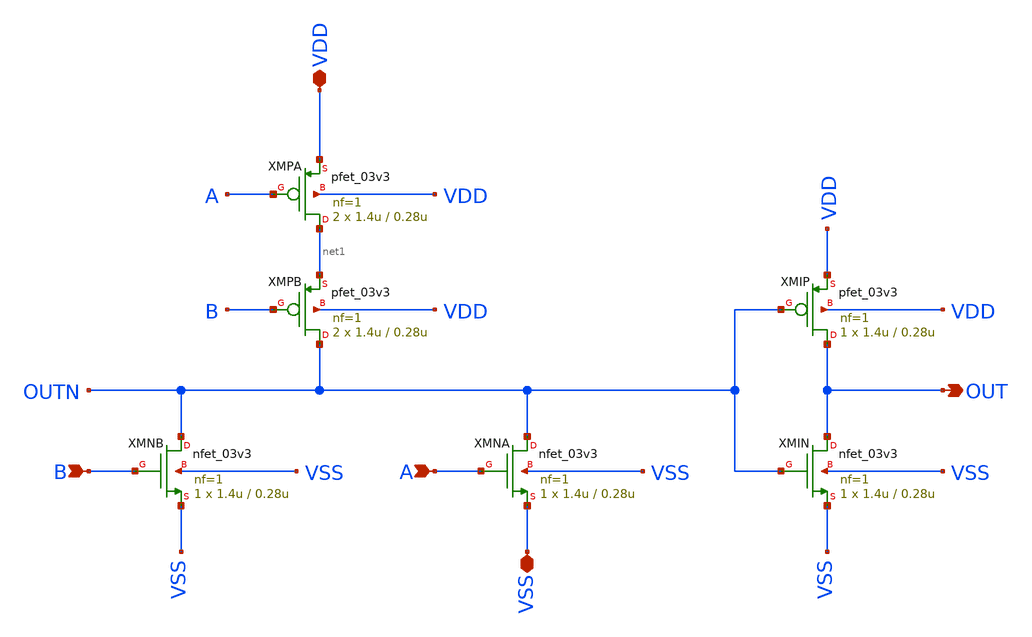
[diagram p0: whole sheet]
** sch_path: designs/gate_or/xschem/gate_or.sch
**.subckt gate_or OUT A VDD VSS B
*.opin OUT
*.ipin A
*.iopin VDD
*.iopin VSS
*.ipin B
XMNB OUTN B VSS VSS nfet_03v3 L=0.28u W=1.4u nf=1 ad='int((nf+1)/2) * W/nf * 0.18u' as='int((nf+2)/2) * W/nf * 0.18u'
+ pd='2*int((nf+1)/2) * (W/nf + 0.18u)' ps='2*int((nf+2)/2) * (W/nf + 0.18u)' nrd='0.18u / W' nrs='0.18u / W'
+ sa=0 sb=0 sd=0 m=1
XMPB OUTN B net1 VDD pfet_03v3 L=0.28u W=1.4u nf=1 ad='int((nf+1)/2) * W/nf * 0.18u' as='int((nf+2)/2) * W/nf * 0.18u'
+ pd='2*int((nf+1)/2) * (W/nf + 0.18u)' ps='2*int((nf+2)/2) * (W/nf + 0.18u)' nrd='0.18u / W' nrs='0.18u / W'
+ sa=0 sb=0 sd=0 m=2
XMNA OUTN A VSS VSS nfet_03v3 L=0.28u W=1.4u nf=1 ad='int((nf+1)/2) * W/nf * 0.18u' as='int((nf+2)/2) * W/nf * 0.18u'
+ pd='2*int((nf+1)/2) * (W/nf + 0.18u)' ps='2*int((nf+2)/2) * (W/nf + 0.18u)' nrd='0.18u / W' nrs='0.18u / W'
+ sa=0 sb=0 sd=0 m=1
XMPA net1 A VDD VDD pfet_03v3 L=0.28u W=1.4u nf=1 ad='int((nf+1)/2) * W/nf * 0.18u' as='int((nf+2)/2) * W/nf * 0.18u'
+ pd='2*int((nf+1)/2) * (W/nf + 0.18u)' ps='2*int((nf+2)/2) * (W/nf + 0.18u)' nrd='0.18u / W' nrs='0.18u / W'
+ sa=0 sb=0 sd=0 m=2
XMIN OUT OUTN VSS VSS nfet_03v3 L=0.28u W=1.4u nf=1 ad='int((nf+1)/2) * W/nf * 0.18u' as='int((nf+2)/2) * W/nf * 0.18u'
+ pd='2*int((nf+1)/2) * (W/nf + 0.18u)' ps='2*int((nf+2)/2) * (W/nf + 0.18u)' nrd='0.18u / W' nrs='0.18u / W'
+ sa=0 sb=0 sd=0 m=1
XMIP OUT OUTN VDD VDD pfet_03v3 L=0.28u W=1.4u nf=1 ad='int((nf+1)/2) * W/nf * 0.18u' as='int((nf+2)/2) * W/nf * 0.18u'
+ pd='2*int((nf+1)/2) * (W/nf + 0.18u)' ps='2*int((nf+2)/2) * (W/nf + 0.18u)' nrd='0.18u / W' nrs='0.18u / W'
+ sa=0 sb=0 sd=0 m=1
**.ends
.end
